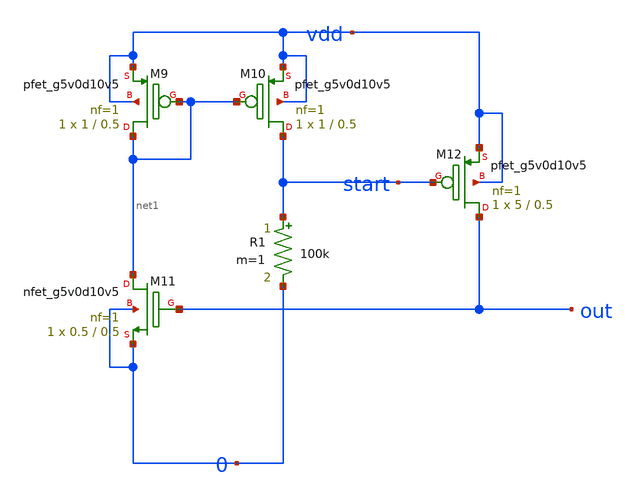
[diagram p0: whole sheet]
** sch_path: Bandgap/My Design/Schematics/Start-up.sch
**.subckt Start-up
XM9 net1 net1 vdd vdd sky130_fd_pr__pfet_g5v0d10v5 L=0.5 W=1 nf=1 ad='int((nf+1)/2) * W/nf * 0.29' as='int((nf+2)/2) * W/nf * 0.29'
+ pd='2*int((nf+1)/2) * (W/nf + 0.29)' ps='2*int((nf+2)/2) * (W/nf + 0.29)' nrd='0.29 / W' nrs='0.29 / W'
+ sa=0 sb=0 sd=0 mult=1 m=1
XM10 start net1 vdd vdd sky130_fd_pr__pfet_g5v0d10v5 L=0.5 W=1 nf=1 ad='int((nf+1)/2) * W/nf * 0.29'
+ as='int((nf+2)/2) * W/nf * 0.29' pd='2*int((nf+1)/2) * (W/nf + 0.29)' ps='2*int((nf+2)/2) * (W/nf + 0.29)'
+ nrd='0.29 / W' nrs='0.29 / W' sa=0 sb=0 sd=0 mult=1 m=1
XM11 net1 out 0 0 sky130_fd_pr__nfet_g5v0d10v5 L=0.5 W=0.5 nf=1 ad='int((nf+1)/2) * W/nf * 0.29' as='int((nf+2)/2) * W/nf * 0.29'
+ pd='2*int((nf+1)/2) * (W/nf + 0.29)' ps='2*int((nf+2)/2) * (W/nf + 0.29)' nrd='0.29 / W' nrs='0.29 / W'
+ sa=0 sb=0 sd=0 mult=1 m=1
R1 start 0 100k m=1
XM12 out start vdd vdd sky130_fd_pr__pfet_g5v0d10v5 L=0.5 W=5 nf=1 ad='int((nf+1)/2) * W/nf * 0.29' as='int((nf+2)/2) * W/nf * 0.29'
+ pd='2*int((nf+1)/2) * (W/nf + 0.29)' ps='2*int((nf+2)/2) * (W/nf + 0.29)' nrd='0.29 / W' nrs='0.29 / W'
+ sa=0 sb=0 sd=0 mult=1 m=1
**.ends
.end
